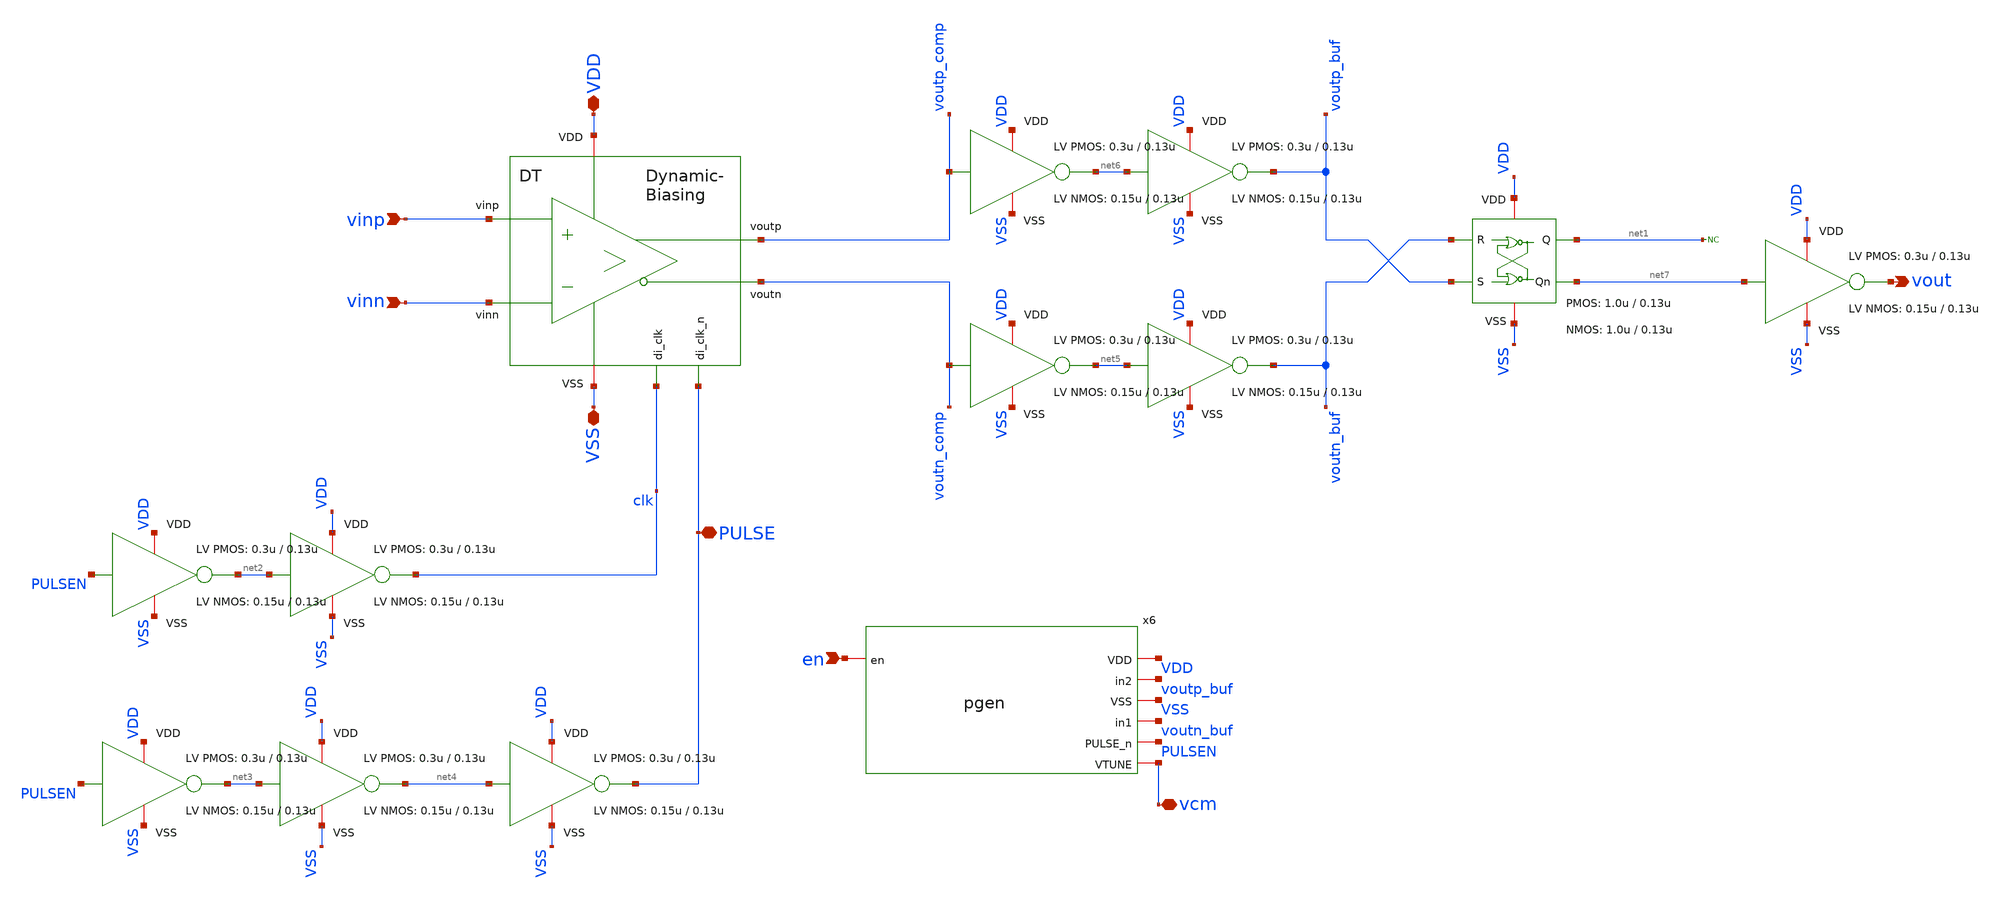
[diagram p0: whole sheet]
** sch_path: xschem/comparator/discrete_time/DT_comparator.sch
**.subckt DT_comparator VDD vout VSS vinp vinn en PULSE vcm
*.iopin VDD
*.opin vout
*.iopin VSS
*.ipin vinp
*.ipin vinn
*.ipin en
*.iopin PULSE
*.iopin vcm
x5 VDD net2 clk VSS inverter_lv W_P=0.3u L_P=0.13u W_N=0.15u L_N=0.13u n=16
* noconn #net1
x4 VDD voutp_buf net7 VSS net1 voutn_buf SR_latch W_P_SR=1.0u L_P_SR=0.13u W_N_SR=1.0u L_N_SR=0.13u
x6 VDD voutp_buf VSS voutn_buf PULSEN vcm en pgen
x1 PULSE clk VDD voutp_comp vinp VSS voutn_comp vinn dynamic_biasing_comparator
x8 VDD PULSEN net2 VSS inverter_lv W_P=0.3u L_P=0.13u W_N=0.15u L_N=0.13u n=4
x9 VDD net3 net4 VSS inverter_lv W_P=0.3u L_P=0.13u W_N=0.15u L_N=0.13u n=16
x10 VDD PULSEN net3 VSS inverter_lv W_P=0.3u L_P=0.13u W_N=0.15u L_N=0.13u n=4
x11 VDD net4 PULSE VSS inverter_lv W_P=0.3u L_P=0.13u W_N=0.15u L_N=0.13u n=64
x12 VDD net5 voutn_buf VSS inverter_lv W_P=0.3u L_P=0.13u W_N=0.15u L_N=0.13u n=8
x13 VDD voutn_comp net5 VSS inverter_lv W_P=0.3u L_P=0.13u W_N=0.15u L_N=0.13u n=2
x2 VDD net6 voutp_buf VSS inverter_lv W_P=0.3u L_P=0.13u W_N=0.15u L_N=0.13u n=8
x3 VDD voutp_comp net6 VSS inverter_lv W_P=0.3u L_P=0.13u W_N=0.15u L_N=0.13u n=2
x7 VDD net7 vout VSS inverter_lv W_P=0.3u L_P=0.13u W_N=0.15u L_N=0.13u n=52
**.ends
.end
